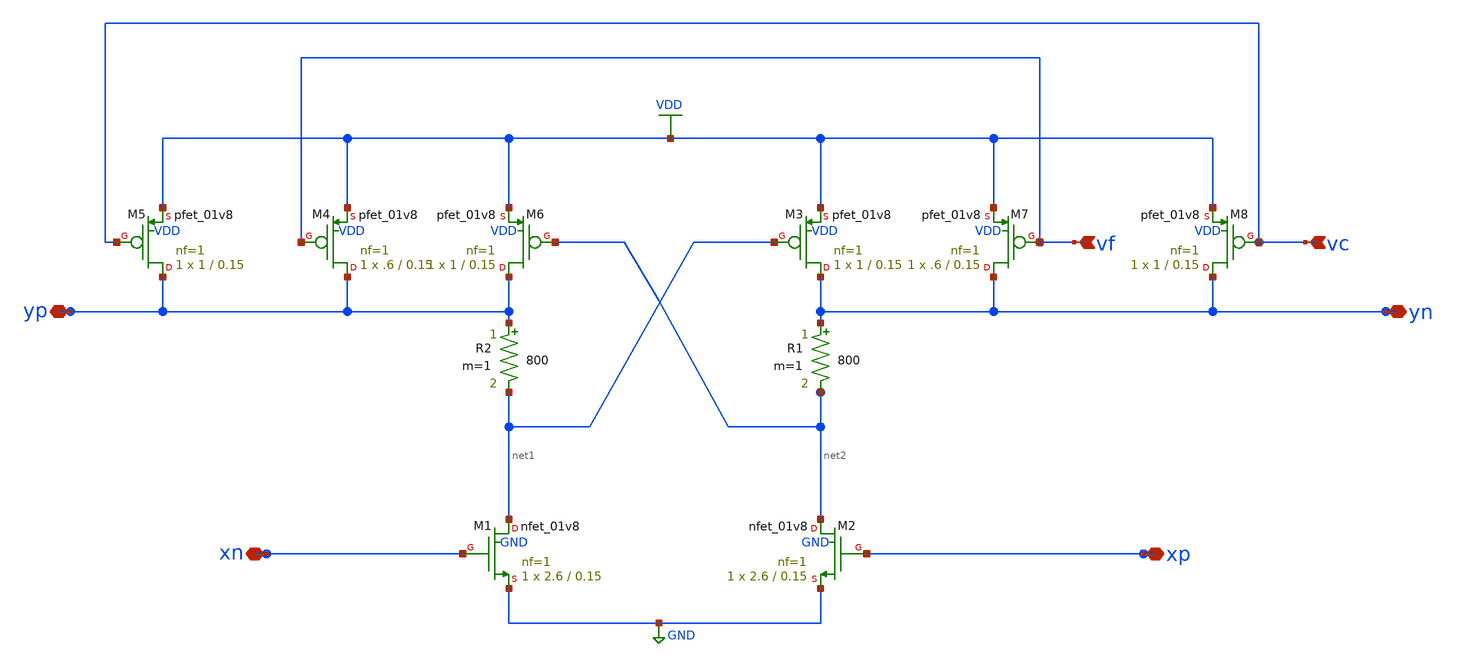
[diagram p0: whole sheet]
** sch_path: Delay_cell_2.sch
**.subckt Delay_cell_2 yp xn xp yn vf vc
*.iopin yp
*.iopin xn
*.iopin xp
*.iopin yn
*.ipin vf
*.ipin vc
R2 yp net1 800 m=1
R1 yn net2 800 m=1
XM1 net1 xn GND GND sky130_fd_pr__nfet_01v8 L=0.15 W=2.6 nf=1 ad='int((nf+1)/2) * W/nf * 0.29' as='int((nf+2)/2) * W/nf * 0.29'
+ pd='2*int((nf+1)/2) * (W/nf + 0.29)' ps='2*int((nf+2)/2) * (W/nf + 0.29)' nrd='0.29 / W' nrs='0.29 / W'
+ sa=0 sb=0 sd=0 mult=1 m=1
XM2 net2 xp GND GND sky130_fd_pr__nfet_01v8 L=0.15 W=2.6 nf=1 ad='int((nf+1)/2) * W/nf * 0.29' as='int((nf+2)/2) * W/nf * 0.29'
+ pd='2*int((nf+1)/2) * (W/nf + 0.29)' ps='2*int((nf+2)/2) * (W/nf + 0.29)' nrd='0.29 / W' nrs='0.29 / W'
+ sa=0 sb=0 sd=0 mult=1 m=1
XM3 yn net1 VDD VDD sky130_fd_pr__pfet_01v8 L=0.15 W=1 nf=1 ad='int((nf+1)/2) * W/nf * 0.29' as='int((nf+2)/2) * W/nf * 0.29'
+ pd='2*int((nf+1)/2) * (W/nf + 0.29)' ps='2*int((nf+2)/2) * (W/nf + 0.29)' nrd='0.29 / W' nrs='0.29 / W'
+ sa=0 sb=0 sd=0 mult=1 m=1
XM4 yp vf VDD VDD sky130_fd_pr__pfet_01v8 L=0.15 W=.6 nf=1 ad='int((nf+1)/2) * W/nf * 0.29' as='int((nf+2)/2) * W/nf * 0.29'
+ pd='2*int((nf+1)/2) * (W/nf + 0.29)' ps='2*int((nf+2)/2) * (W/nf + 0.29)' nrd='0.29 / W' nrs='0.29 / W'
+ sa=0 sb=0 sd=0 mult=1 m=1
XM5 yp vc VDD VDD sky130_fd_pr__pfet_01v8 L=0.15 W=1 nf=1 ad='int((nf+1)/2) * W/nf * 0.29' as='int((nf+2)/2) * W/nf * 0.29'
+ pd='2*int((nf+1)/2) * (W/nf + 0.29)' ps='2*int((nf+2)/2) * (W/nf + 0.29)' nrd='0.29 / W' nrs='0.29 / W'
+ sa=0 sb=0 sd=0 mult=1 m=1
XM6 yp net2 VDD VDD sky130_fd_pr__pfet_01v8 L=0.15 W=1 nf=1 ad='int((nf+1)/2) * W/nf * 0.29' as='int((nf+2)/2) * W/nf * 0.29'
+ pd='2*int((nf+1)/2) * (W/nf + 0.29)' ps='2*int((nf+2)/2) * (W/nf + 0.29)' nrd='0.29 / W' nrs='0.29 / W'
+ sa=0 sb=0 sd=0 mult=1 m=1
XM7 yn vf VDD VDD sky130_fd_pr__pfet_01v8 L=0.15 W=.6 nf=1 ad='int((nf+1)/2) * W/nf * 0.29' as='int((nf+2)/2) * W/nf * 0.29'
+ pd='2*int((nf+1)/2) * (W/nf + 0.29)' ps='2*int((nf+2)/2) * (W/nf + 0.29)' nrd='0.29 / W' nrs='0.29 / W'
+ sa=0 sb=0 sd=0 mult=1 m=1
XM8 yn vc VDD VDD sky130_fd_pr__pfet_01v8 L=0.15 W=1 nf=1 ad='int((nf+1)/2) * W/nf * 0.29' as='int((nf+2)/2) * W/nf * 0.29'
+ pd='2*int((nf+1)/2) * (W/nf + 0.29)' ps='2*int((nf+2)/2) * (W/nf + 0.29)' nrd='0.29 / W' nrs='0.29 / W'
+ sa=0 sb=0 sd=0 mult=1 m=1
**.ends
.GLOBAL GND
.GLOBAL VDD
.end
